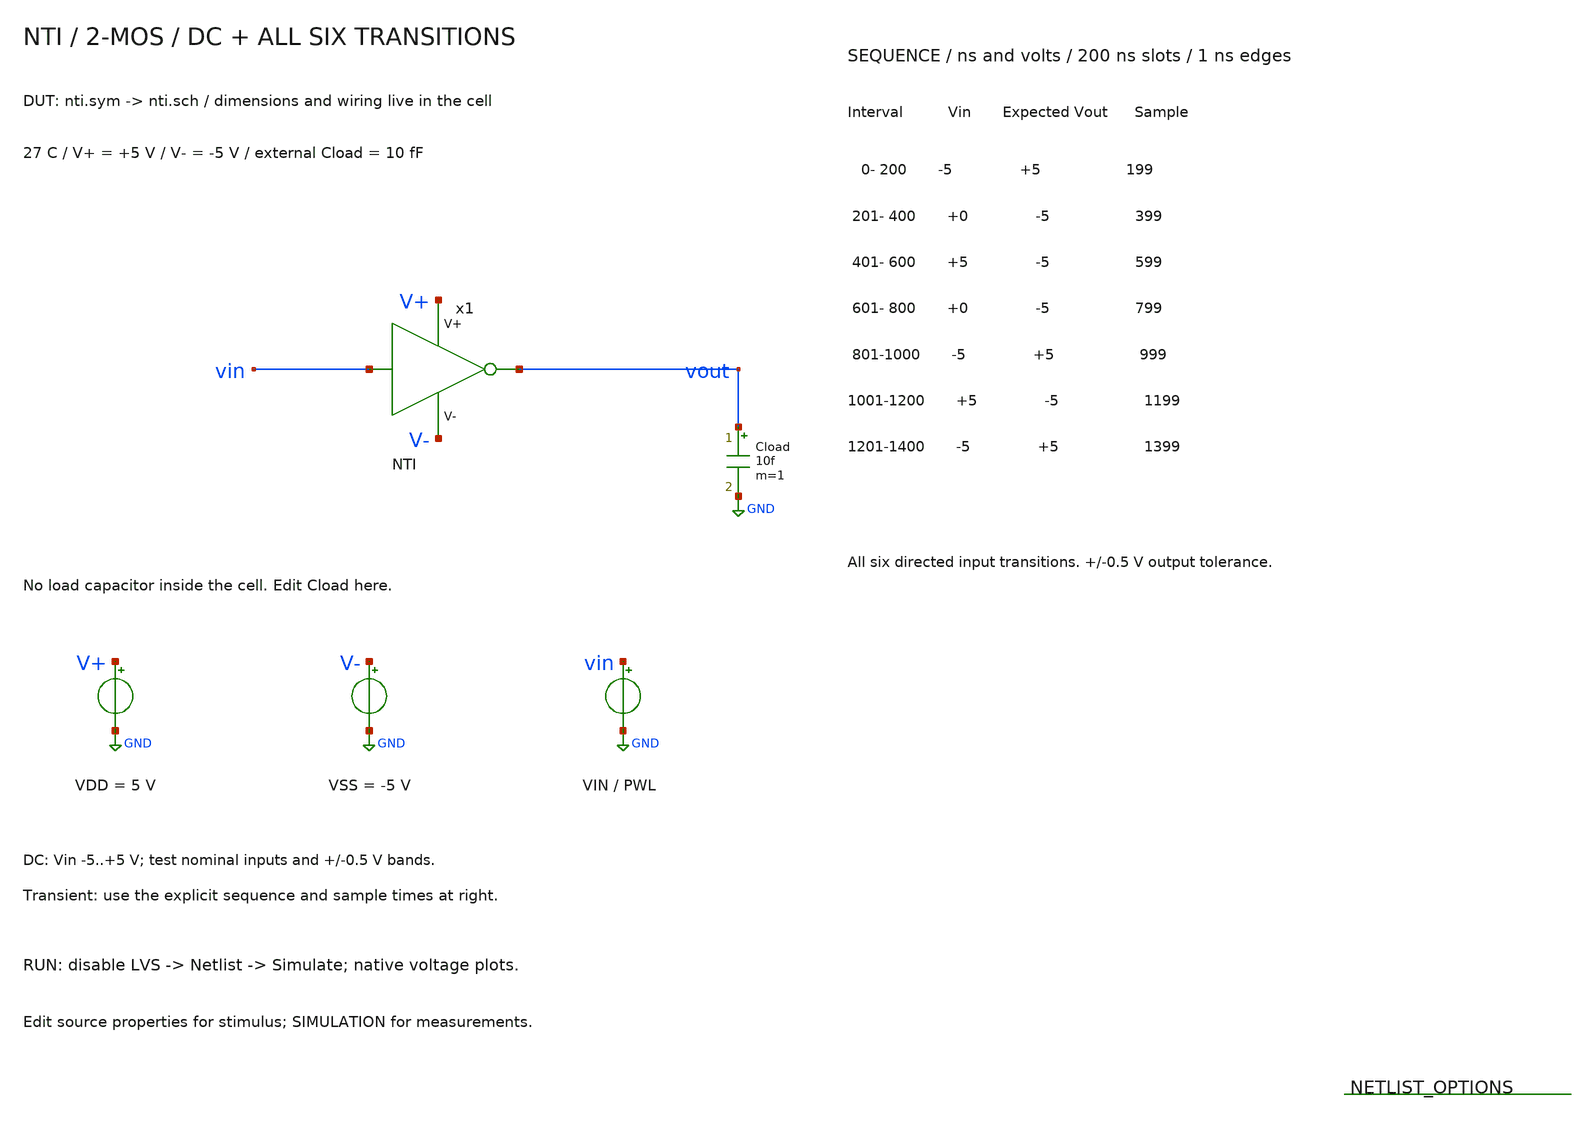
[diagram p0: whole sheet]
** sch_path: member_project/balanced-ternary-logic/PenguinEino/nti_tb.sch
**.subckt nti_tb
x1 vin vout V+ V- nti
Cload vout GND 10f m=1
VDD V+ GND 5
VSS V- GND -5
VIN vin GND PWL(0 -5 200n -5 201n 0 400n 0 401n 5 600n 5 601n 0 800n 0 801n -5 1000n -5 1001n 5
+ 1200n 5 1201n -5 1400n -5)
**** begin user architecture code
 .include $::LIB/ip62_models

.temp 27
.options rshunt=1e12
.control
save all
set wr_singlescale
set wr_vecnames
setplot const
let failures=0
dc VIN -5 5 0.015625
meas dc dc_0 find v(vout) at=-5
if abs(dc_0-(5)) > 0.5
let const.failures=const.failures+1
echo FAIL: dc_0 expected 5 V
end
meas dc dc_1 find v(vout) at=-4.5
if abs(dc_1-(5)) > 0.5
let const.failures=const.failures+1
echo FAIL: dc_1 expected 5 V
end
meas dc dc_2 find v(vout) at=-0.5
if abs(dc_2-(-5)) > 0.5
let const.failures=const.failures+1
echo FAIL: dc_2 expected -5 V
end
meas dc dc_3 find v(vout) at=0
if abs(dc_3-(-5)) > 0.5
let const.failures=const.failures+1
echo FAIL: dc_3 expected -5 V
end
meas dc dc_4 find v(vout) at=0.5
if abs(dc_4-(-5)) > 0.5
let const.failures=const.failures+1
echo FAIL: dc_4 expected -5 V
end
meas dc dc_5 find v(vout) at=4.5
if abs(dc_5-(-5)) > 0.5
let const.failures=const.failures+1
echo FAIL: dc_5 expected -5 V
end
meas dc dc_6 find v(vout) at=5
if abs(dc_6-(-5)) > 0.5
let const.failures=const.failures+1
echo FAIL: dc_6 expected -5 V
end
plot v(vin) v(vout) title 'NTI: DC transfer'
wrdata nti_dc.txt v(vin) v(vout)
reset
tran 0.05n 1400n
let expected=5-10*(v(vin)>-2.5)
plot v(vin) v(vout) expected title 'NTI: all six input transitions'
wrdata nti_tran.txt v(vin) v(vout)
meas tran tran_0 find v(vout) at=199n
if abs(tran_0-(5)) > 0.5
let const.failures=const.failures+1
echo FAIL: tran_0 expected 5 V
end
meas tran tran_1 find v(vout) at=399n
if abs(tran_1-(-5)) > 0.5
let const.failures=const.failures+1
echo FAIL: tran_1 expected -5 V
end
meas tran tran_2 find v(vout) at=599n
if abs(tran_2-(-5)) > 0.5
let const.failures=const.failures+1
echo FAIL: tran_2 expected -5 V
end
meas tran tran_3 find v(vout) at=799n
if abs(tran_3-(-5)) > 0.5
let const.failures=const.failures+1
echo FAIL: tran_3 expected -5 V
end
meas tran tran_4 find v(vout) at=999n
if abs(tran_4-(5)) > 0.5
let const.failures=const.failures+1
echo FAIL: tran_4 expected 5 V
end
meas tran tran_5 find v(vout) at=1199n
if abs(tran_5-(-5)) > 0.5
let const.failures=const.failures+1
echo FAIL: tran_5 expected -5 V
end
meas tran tran_6 find v(vout) at=1399n
if abs(tran_6-(5)) > 0.5
let const.failures=const.failures+1
echo FAIL: tran_6 expected 5 V
end
if const.failures = 0
echo PASS: NTI DC bands and transient samples
else
echo FAIL: NTI samples outside +/-0.5 V
end
print const.failures
.endc

**** end user architecture code
**.ends

* expanding   symbol:  /home/ishi-kai/balanced-ternary-logic/nti.sym # of pins=4
** sym_path: member_project/balanced-ternary-logic/PenguinEino/nti.sym
** sch_path: member_project/balanced-ternary-logic/PenguinEino/nti.sch
.subckt nti vin vout V+ V-
*.iopin V+
*.opin vout
*.ipin vin
*.iopin V-
XXM1 vout vin V+ V+ PMOS w=3.4u l=1u nrd=0 nrs=0 m=1
XXM2 vout vin V- V- NMOS w=7u l=1u nrd=0 nrs=0 m=1
.ends

.GLOBAL GND
.end
